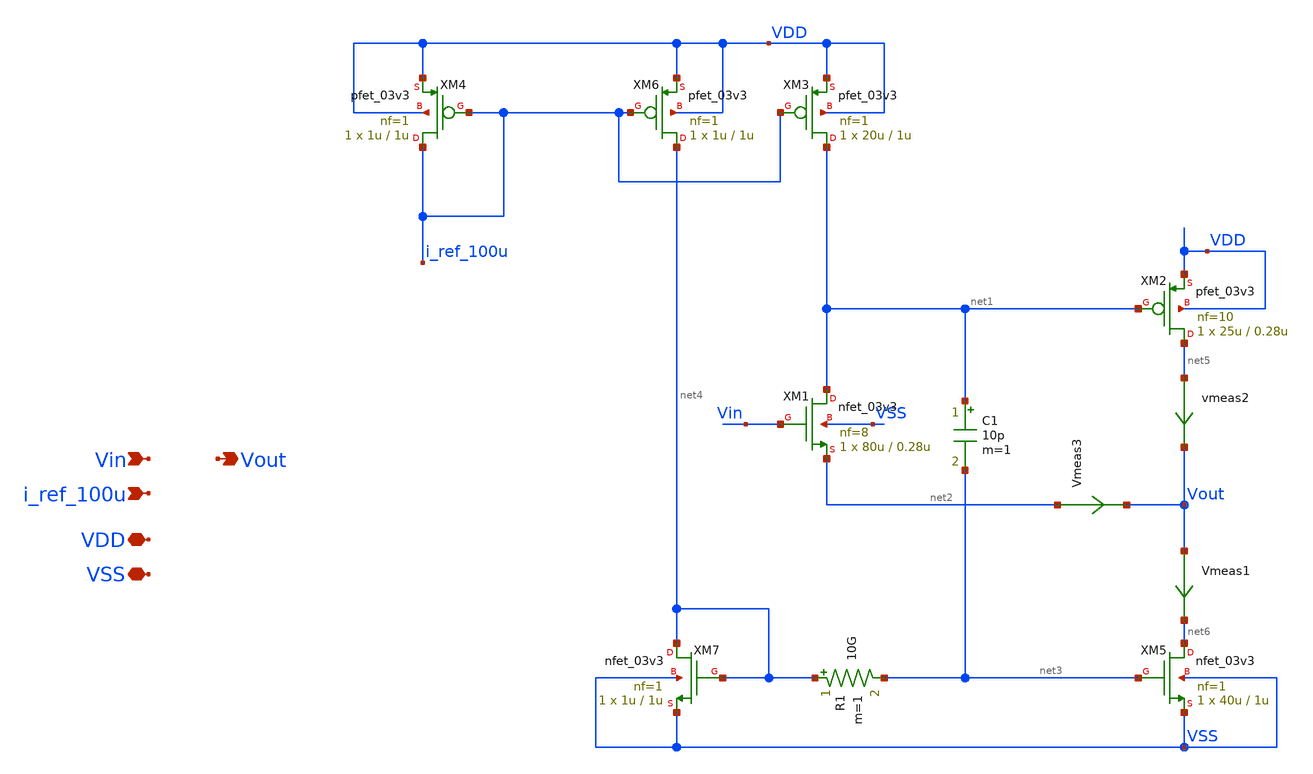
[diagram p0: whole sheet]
** sch_path: designs/output_buffer/schematic/output_buffer.sch
**.subckt output_buffer Vin Vout i_ref_100u VDD VSS
*.ipin Vin
*.opin Vout
*.ipin i_ref_100u
*.iopin VDD
*.iopin VSS
XM1 net1 Vin net2 VSS nfet_03v3 L=0.28u W=80u nf=8 ad='int((nf+1)/2) * W/nf * 0.18u' as='int((nf+2)/2) * W/nf * 0.18u'
+ pd='2*int((nf+1)/2) * (W/nf + 0.18u)' ps='2*int((nf+2)/2) * (W/nf + 0.18u)' nrd='0.18u / W' nrs='0.18u / W'
+ sa=0 sb=0 sd=0 m=1
XM2 net5 net1 VDD VDD pfet_03v3 L=0.28u W=25u nf=10 ad='int((nf+1)/2) * W/nf * 0.18u' as='int((nf+2)/2) * W/nf * 0.18u'
+ pd='2*int((nf+1)/2) * (W/nf + 0.18u)' ps='2*int((nf+2)/2) * (W/nf + 0.18u)' nrd='0.18u / W' nrs='0.18u / W'
+ sa=0 sb=0 sd=0 m=1
XM3 net1 i_ref_100u VDD VDD pfet_03v3 L=1u W=20u nf=1 ad='int((nf+1)/2) * W/nf * 0.18u' as='int((nf+2)/2) * W/nf * 0.18u'
+ pd='2*int((nf+1)/2) * (W/nf + 0.18u)' ps='2*int((nf+2)/2) * (W/nf + 0.18u)' nrd='0.18u / W' nrs='0.18u / W'
+ sa=0 sb=0 sd=0 m=1
XM4 i_ref_100u i_ref_100u VDD VDD pfet_03v3 L=1u W=1u nf=1 ad='int((nf+1)/2) * W/nf * 0.18u' as='int((nf+2)/2) * W/nf * 0.18u'
+ pd='2*int((nf+1)/2) * (W/nf + 0.18u)' ps='2*int((nf+2)/2) * (W/nf + 0.18u)' nrd='0.18u / W' nrs='0.18u / W'
+ sa=0 sb=0 sd=0 m=1
XM5 net6 net3 VSS VSS nfet_03v3 L=1u W=40u nf=1 ad='int((nf+1)/2) * W/nf * 0.18u' as='int((nf+2)/2) * W/nf * 0.18u'
+ pd='2*int((nf+1)/2) * (W/nf + 0.18u)' ps='2*int((nf+2)/2) * (W/nf + 0.18u)' nrd='0.18u / W' nrs='0.18u / W'
+ sa=0 sb=0 sd=0 m=1
R1 net4 net3 10G m=1
vmeas2 net5 Vout 0
.save i(vmeas2)
Vmeas1 Vout net6 0
.save i(vmeas1)
C1 net1 net3 10p m=1
XM6 net4 i_ref_100u VDD VDD pfet_03v3 L=1u W=1u nf=1 ad='int((nf+1)/2) * W/nf * 0.18u' as='int((nf+2)/2) * W/nf * 0.18u'
+ pd='2*int((nf+1)/2) * (W/nf + 0.18u)' ps='2*int((nf+2)/2) * (W/nf + 0.18u)' nrd='0.18u / W' nrs='0.18u / W'
+ sa=0 sb=0 sd=0 m=1
XM7 net4 net4 VSS VSS nfet_03v3 L=1u W=1u nf=1 ad='int((nf+1)/2) * W/nf * 0.18u' as='int((nf+2)/2) * W/nf * 0.18u'
+ pd='2*int((nf+1)/2) * (W/nf + 0.18u)' ps='2*int((nf+2)/2) * (W/nf + 0.18u)' nrd='0.18u / W' nrs='0.18u / W'
+ sa=0 sb=0 sd=0 m=1
Vmeas3 net2 Vout 0
.save i(vmeas3)
**.ends
.end
